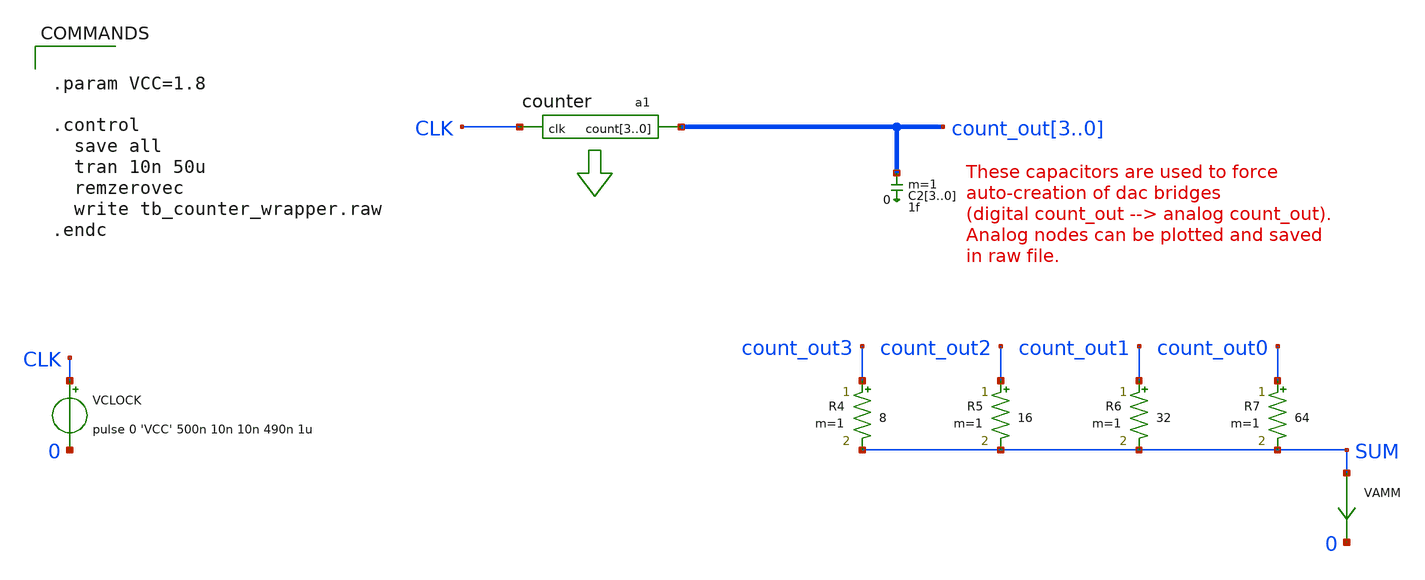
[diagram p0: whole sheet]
** sch_path: xschem_library/ngspice_verilog_cosim/tb_counter_wrapper.sch
**.subckt tb_counter_wrapper
VCLOCK CLK 0 pulse 0 'VCC' 500n 10n 10n 490n 1u
a1 [ CLK ] [ count_out3 count_out2 count_out1 count_out0 ] counter
C23 count_out3 0 1f m=1
C22 count_out2 0 1f m=1
C21 count_out1 0 1f m=1
C20 count_out0 0 1f m=1
VAMM SUM 0 0
R4 count_out3 SUM 8 m=1
R5 count_out2 SUM 16 m=1
R6 count_out1 SUM 32 m=1
R7 count_out0 SUM 64 m=1
**** begin user architecture code


.param VCC=1.8

.control
  save all
  tran 10n 50u
  remzerovec
  write tb_counter_wrapper.raw
.endc


**** end user architecture code
**.ends
**** begin user architecture code
.model counter d_cosim simulation="ivlng" sim_args=["counter"]
**** end user architecture code
.end
